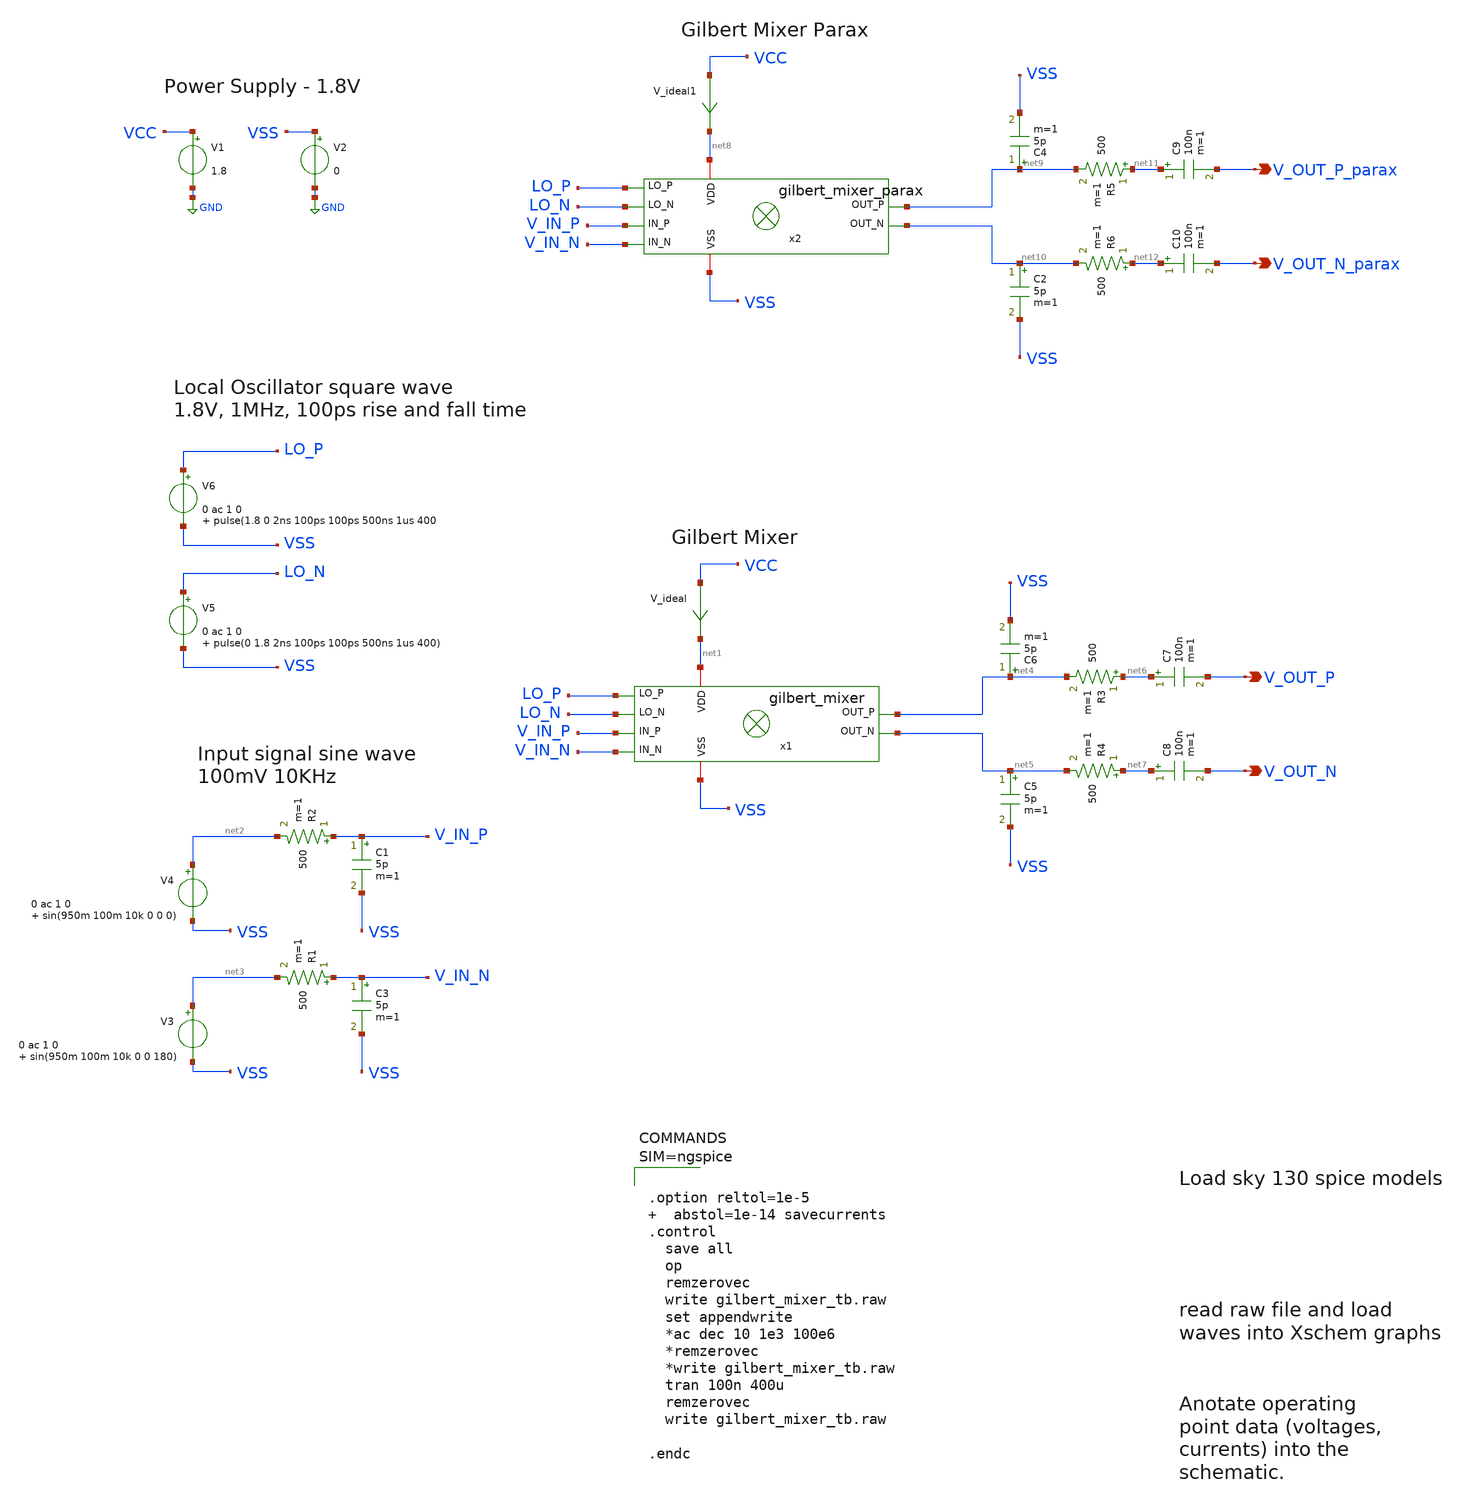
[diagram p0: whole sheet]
** sch_path: xschem/gilbert_mixer_tb.sch
**.subckt gilbert_mixer_tb V_OUT_N V_OUT_P V_OUT_N_parax V_OUT_P_parax
*.opin V_OUT_N
*.opin V_OUT_P
*.opin V_OUT_N_parax
*.opin V_OUT_P_parax
V1 VCC GND 1.8
V2 VSS GND 0
V4 net2 VSS 0 ac 1 0 sin(950m 100m 10k 0 0 0)
x1 VSS net1 net5 net4 LO_N LO_P V_IN_N V_IN_P gilbert_mixer
V5 LO_N VSS 0 ac 1 0 pulse(0 1.8 2ns 100ps 100ps 500ns 1us 400)
V3 net3 VSS 0 ac 1 0 sin(950m 100m 10k 0 0 180)
V_ideal VCC net1 0
.save i(v_ideal)
V6 LO_P VSS 0 ac 1 0 pulse(1.8 0 2ns 100ps 100ps 500ns 1us 400
R1 V_IN_N net3 500 m=1
R2 V_IN_P net2 500 m=1
R3 net6 net4 500 m=1
R4 net7 net5 500 m=1
C1 V_IN_P VSS 5p m=1
C3 V_IN_N VSS 5p m=1
C5 net5 VSS 5p m=1
C6 net4 VSS 5p m=1
C7 net6 V_OUT_P 100n m=1
C8 net7 V_OUT_N 100n m=1
x2 VSS net8 net10 net9 LO_N LO_P V_IN_N V_IN_P gilbert_mixer_parax
V_ideal1 VCC net8 0
.save i(v_ideal1)
R5 net11 net9 500 m=1
R6 net12 net10 500 m=1
C2 net10 VSS 5p m=1
C4 net9 VSS 5p m=1
C9 net11 V_OUT_P_parax 100n m=1
C10 net12 V_OUT_N_parax 100n m=1
**** begin user architecture code

** opencircuitdesign pdks install
.lib $::SKYWATER_MODELS/sky130.lib.spice tt





.option reltol=1e-5   abstol=1e-14 savecurrents
.control
  save all
  op
  remzerovec
  write gilbert_mixer_tb.raw
  set appendwrite
  *ac dec 10 1e3 100e6
  *remzerovec
  *write gilbert_mixer_tb.raw
  tran 100n 400u
  remzerovec
  write gilbert_mixer_tb.raw

.endc



**** end user architecture code
**.ends

* expanding   symbol:  gilbert_mixer.sym # of pins=8
** sym_path: xschem/gilbert_mixer.sym
** sch_path: xschem/gilbert_mixer.sch
.subckt gilbert_mixer VSS VDD OUT_N OUT_P LO_N LO_P IN_N IN_P
*.iopin VDD
*.iopin VSS
*.ipin LO_P
*.ipin LO_N
*.ipin IN_P
*.ipin IN_N
*.opin OUT_N
*.opin OUT_P
XR3 VSS NET_R3 net2 sky130_fd_pr__res_high_po_0p35 L=0.1 mult=15 m=15
XM2 OUT_P IN_N NET_M6_DRAIN VSS sky130_fd_pr__nfet_01v8 L=0.38 W=3.6 nf=2 ad='int((nf+1)/2) * W/nf * 0.29'
+ as='int((nf+2)/2) * W/nf * 0.29' pd='2*int((nf+1)/2) * (W/nf + 0.29)' ps='2*int((nf+2)/2) * (W/nf + 0.29)'
+ nrd='0.29 / W' nrs='0.29 / W' sa=0 sb=0 sd=0 mult=1 m=1
XM4 OUT_N IN_N NET_M5_DRAIN VSS sky130_fd_pr__nfet_01v8 L=0.38 W=3.6 nf=2 ad='int((nf+1)/2) * W/nf * 0.29'
+ as='int((nf+2)/2) * W/nf * 0.29' pd='2*int((nf+1)/2) * (W/nf + 0.29)' ps='2*int((nf+2)/2) * (W/nf + 0.29)'
+ nrd='0.29 / W' nrs='0.29 / W' sa=0 sb=0 sd=0 mult=1 m=1
XM6 NET_M6_DRAIN LO_N NET_R3 VSS sky130_fd_pr__nfet_01v8 L=0.38 W=3.6 nf=2 ad='int((nf+1)/2) * W/nf * 0.29'
+ as='int((nf+2)/2) * W/nf * 0.29' pd='2*int((nf+1)/2) * (W/nf + 0.29)' ps='2*int((nf+2)/2) * (W/nf + 0.29)'
+ nrd='0.29 / W' nrs='0.29 / W' sa=0 sb=0 sd=0 mult=1 m=1
XM1 OUT_N IN_P NET_M6_DRAIN VSS sky130_fd_pr__nfet_01v8 L=0.38 W=3.6 nf=2 ad='int((nf+1)/2) * W/nf * 0.29'
+ as='int((nf+2)/2) * W/nf * 0.29' pd='2*int((nf+1)/2) * (W/nf + 0.29)' ps='2*int((nf+2)/2) * (W/nf + 0.29)'
+ nrd='0.29 / W' nrs='0.29 / W' sa=0 sb=0 sd=0 mult=1 m=1
XM3 OUT_P IN_P NET_M5_DRAIN VSS sky130_fd_pr__nfet_01v8 L=0.38 W=3.6 nf=2 ad='int((nf+1)/2) * W/nf * 0.29'
+ as='int((nf+2)/2) * W/nf * 0.29' pd='2*int((nf+1)/2) * (W/nf + 0.29)' ps='2*int((nf+2)/2) * (W/nf + 0.29)'
+ nrd='0.29 / W' nrs='0.29 / W' sa=0 sb=0 sd=0 mult=1 m=1
XM5 NET_M5_DRAIN LO_P NET_R3 VSS sky130_fd_pr__nfet_01v8 L=0.38 W=3.6 nf=2 ad='int((nf+1)/2) * W/nf * 0.29'
+ as='int((nf+2)/2) * W/nf * 0.29' pd='2*int((nf+1)/2) * (W/nf + 0.29)' ps='2*int((nf+2)/2) * (W/nf + 0.29)'
+ nrd='0.29 / W' nrs='0.29 / W' sa=0 sb=0 sd=0 mult=1 m=1
XR2 OUT_P VDD net1 sky130_fd_pr__res_high_po_0p35 L=2.3 mult=1 m=1
XR1 OUT_N VDD VSS sky130_fd_pr__res_high_po_0p35 L=2.3 mult=1 m=1
.ends


* expanding   symbol:  gilbert_mixer_parax.sym # of pins=8
** sym_path: xschem/gilbert_mixer.sym
.include [file normalize ../mag/gilbert_mixer.sim.spice]
.GLOBAL GND
.end
